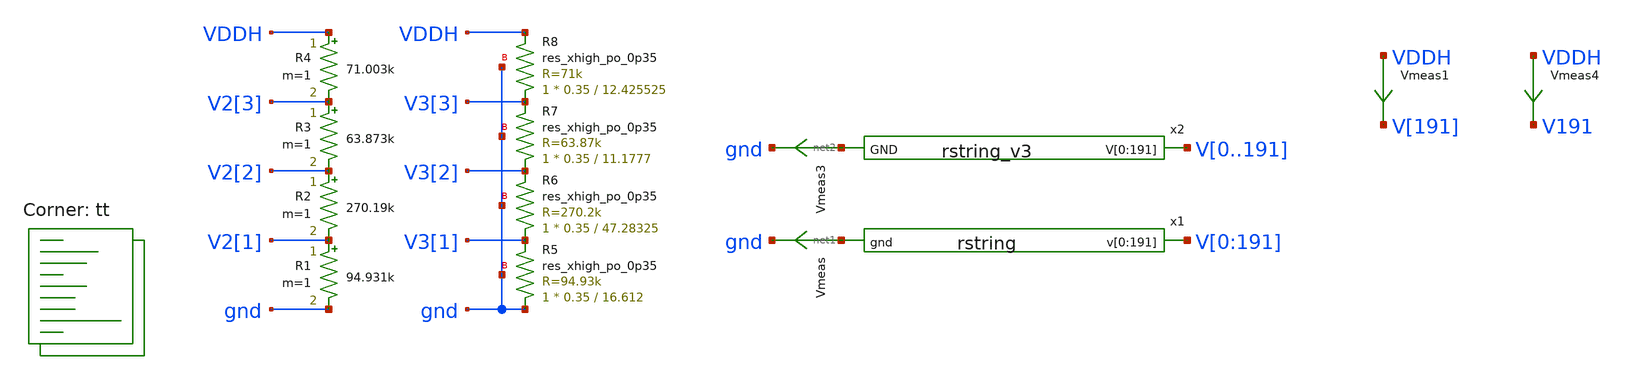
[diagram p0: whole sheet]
** sch_path: xschem/res_seg-tb.sch
**.subckt res_seg-tb
x1 V[0] V[1] V[2] V[3] V[4] V[5] V[6] V[7] V[8] V[9] V[10] V[11] V[12] V[13] V[14] V[15] V[16] V[17]
+ V[18] V[19] V[20] V[21] V[22] V[23] V[24] V[25] V[26] V[27] V[28] V[29] V[30] V[31] V[32] V[33] V[34]
+ V[35] V[36] V[37] V[38] V[39] V[40] V[41] V[42] V[43] V[44] V[45] V[46] V[47] V[48] V[49] V[50] V[51]
+ V[52] V[53] V[54] V[55] V[56] V[57] V[58] V[59] V[60] V[61] V[62] V[63] V[64] V[65] V[66] V[67] V[68]
+ V[69] V[70] V[71] V[72] V[73] V[74] V[75] V[76] V[77] V[78] V[79] V[80] V[81] V[82] V[83] V[84] V[85]
+ V[86] V[87] V[88] V[89] V[90] V[91] V[92] V[93] V[94] V[95] V[96] V[97] V[98] V[99] V[100] V[101] V[102]
+ V[103] V[104] V[105] V[106] V[107] V[108] V[109] V[110] V[111] V[112] V[113] V[114] V[115] V[116] V[117]
+ V[118] V[119] V[120] V[121] V[122] V[123] V[124] V[125] V[126] V[127] V[128] V[129] V[130] V[131] V[132]
+ V[133] V[134] V[135] V[136] V[137] V[138] V[139] V[140] V[141] V[142] V[143] V[144] V[145] V[146] V[147]
+ V[148] V[149] V[150] V[151] V[152] V[153] V[154] V[155] V[156] V[157] V[158] V[159] V[160] V[161] V[162]
+ V[163] V[164] V[165] V[166] V[167] V[168] V[169] V[170] V[171] V[172] V[173] V[174] V[175] V[176] V[177]
+ V[178] V[179] V[180] V[181] V[182] V[183] V[184] V[185] V[186] V[187] V[188] V[189] V[190] V[191] net1
+ rstring
Vmeas net1 gnd 0
.save i(vmeas)
Vmeas1 VDDH V[191] 0
.save i(vmeas1)
R1 V2[1] gnd 94.931k m=1
R2 V2[2] V2[1] 270.19k m=1
R3 V2[3] V2[2] 63.873k m=1
R4 VDDH V2[3] 71.003k m=1
XR5 gnd V3[1] gnd sky130_fd_pr__res_xhigh_po_0p35 L=16.612 mult=1 m=1
XR6 V3[1] V3[2] gnd sky130_fd_pr__res_xhigh_po_0p35 L=47.28325 mult=1 m=1
XR7 V3[2] V3[3] gnd sky130_fd_pr__res_xhigh_po_0p35 L=11.1777 mult=1 m=1
XR8 V3[3] VDDH gnd sky130_fd_pr__res_xhigh_po_0p35 L=12.425525 mult=1 m=1
Vmeas3 net2 gnd 0
.save i(vmeas3)
x2 V0 V1 V2 V3 V4 V5 V6 V7 V8 V9 V10 V11 V12 V13 V14 V15 V16 V17 V18 V19 V20 V21 V22 V23 V24 V25 V26
+ V27 V28 V29 V30 V31 V32 V33 V34 V35 V36 V37 V38 V39 V40 V41 V42 V43 V44 V45 V46 V47 V48 V49 V50 V51 V52
+ V53 V54 V55 V56 V57 V58 V59 V60 V61 V62 V63 V64 V65 V66 V67 V68 V69 V70 V71 V72 V73 V74 V75 V76 V77 V78
+ V79 V80 V81 V82 V83 V84 V85 V86 V87 V88 V89 V90 V91 V92 V93 V94 V95 V96 V97 V98 V99 V100 V101 V102 V103
+ V104 V105 V106 V107 V108 V109 V110 V111 V112 V113 V114 V115 V116 V117 V118 V119 V120 V121 V122 V123 V124
+ V125 V126 V127 V128 V129 V130 V131 V132 V133 V134 V135 V136 V137 V138 V139 V140 V141 V142 V143 V144 V145
+ V146 V147 V148 V149 V150 V151 V152 V153 V154 V155 V156 V157 V158 V159 V160 V161 V162 V163 V164 V165 V166
+ V167 V168 V169 V170 V171 V172 V173 V174 V175 V176 V177 V178 V179 V180 V181 V182 V183 V184 V185 V186 V187
+ V188 V189 V190 V191 net2 rstring_v3
Vmeas4 VDDH V191 0
.save i(vmeas4)
**** begin user architecture code



  .include $THESIS_WS/spice/header.spice
  .option wnflag=1
  .option safecurrents
  ********************Static Voltage Sources***************************
  Vddh vddh gnd dc 5.5
  v0 v[0] gnd 0
  *v191 v[191] gnd 5.5

  *v1_191 v1[191] gnd 5.5
  v1_0 v0 gnd 0

  Vdm dm gnd 0
  ********************Dynamic Voltage Sources***************************
  *******Calculation**********
  .param base_f=100e3 base_t={1/base_f} base_th={base_t/2} base_d={base_th}
  .param d2_th ={base_th} d2_t={d1_th}
  .param d1_th ={4*d2_th} d1_t={d0_th}
  .param d0_th ={4*d1_th} d0_t={4*d0_th}

  .param d20_d ={0} d21_d={1*d2_th} d22_d={2*d2_th} d23_d={3*d2_th}
  .param d10_d ={0} d11_d={1*d1_th} d12_d={2*d1_th} d13_d={3*d1_th}
  .param d00_d ={0} d01_d={1*d0_th} d02_d={2*d0_th} d03_d={3*d0_th}
  *******Signals**********
  .param vhi=5.5
 * Vd00 d0[0] gnd pulse(0 {vhi} {d00_d} 1n 1n {d0_th} {d0_t})
 * Vd01 d0[1] gnd pulse(0 {vhi} {d01_d} 1n 1n {d0_th} {d0_t})
 * Vd02 d0[2] gnd pulse(0 {vhi} {d02_d} 1n 1n {d0_th} {d0_t})
 * Vd03 d0[3] gnd pulse(0 {vhi} {d03_d} 1n 1n {d0_th} {d0_t})

 * Vd10 d1[0] gnd pulse(0 {vhi} {d10_d} 1n 1n {d1_th} {d1_t})
 * Vd11 d1[1] gnd pulse(0 {vhi} {d11_d} 1n 1n {d1_th} {d1_t})
 * Vd12 d1[2] gnd pulse(0 {vhi} {d12_d} 1n 1n {d1_th} {d1_t})
 * Vd13 d1[3] gnd pulse(0 {vhi} {d13_d} 1n 1n {d1_th} {d1_t})

 * Vd20 d2[0] gnd pulse(0 {vhi} {d20_d} 1n 1n {d2_th} {d2_t})
 * Vd21 d2[1] gnd pulse(0 {vhi} {d21_d} 1n 1n {d2_th} {d2_t})
 * Vd22 d2[2] gnd pulse(0 {vhi} {d22_d} 1n 1n {d2_th} {d2_t})
 * Vd23 d2[3] gnd pulse(0 {vhi} {d23_d} 1n 1n {d2_th} {d2_t})
  ********************Simulation Commands*****************************
  .control
     reset
     *save all
     *tran 1u 10u
     dc Vdm 0 1 1
     write res_seg-tb.raw
     set wr_singlescale
     set wr_vecnames
     wrdata $THESIS_WS/simulations/rseg-tb11.txt dc.all


*     dc Vdm 0 1 1
*     write res_seg-tb.raw
*    quit 0
  .endc



.lib $::SKYWATER_MODELS/sky130.lib.spice tt


.save v1 v2 v3 v4 v5 v6 v7 v8 v9 v10
.save v11 v12 v13 v14 v15 v16 v17 v18 v19 v20
.save v21 v22 v23 v24 v25 v26 v27 v28 v29 v30
.save v31 v32 v33 v34 v35 v36 v37 v38 v39 v40
.save v41 v42 v43 v44 v45 v46 v47 v48 v49 v50
.save v51 v52 v53 v54 v55 v56 v57 v58 v59 v60
.save v61 v62 v63 v64 v65 v66 v67 v68 v69 v70
.save v71 v72 v73 v74 v75 v76 v77 v78 v79 v80
.save v81 v82 v83 v84 v85 v86 v87 v88 v89 v90
.save v91 v92 v93 v94 v95 v96 v97 v98 v99 v100
.save v101 v102 v103 v104 v105 v106 v107 v108 v109 v110
.save v111 v112 v113 v114 v115 v116 v117 v118 v119 v120
.save v121 v122 v123 v124 v125 v126 v127 v128 v129 v130
.save v131 v132 v133 v134 v135 v136 v137 v138 v139 v140
.save v141 v142 v143 v144 v145 v146 v147 v148 v149 v150
.save v151 v152 v153 v154 v155 v156 v157 v158 v159 v160
.save v161 v162 v163 v164 v165 v166 v167 v168 v169 v170
.save v171 v172 v173 v174 v175 v176 v177 v178 v179 v180
.save v181 v182 v183 v184 v185 v186 v187 v188 v189 v190
.save v191


**** end user architecture code
**.ends

* expanding   symbol:  rstring.sym # of pins=2
** sym_path: xschem/rstring.sym
** sch_path: xschem/rstring.sch
.subckt rstring v[0] v[1] v[2] v[3] v[4] v[5] v[6] v[7] v[8] v[9] v[10] v[11] v[12] v[13] v[14]
+ v[15] v[16] v[17] v[18] v[19] v[20] v[21] v[22] v[23] v[24] v[25] v[26] v[27] v[28] v[29] v[30] v[31]
+ v[32] v[33] v[34] v[35] v[36] v[37] v[38] v[39] v[40] v[41] v[42] v[43] v[44] v[45] v[46] v[47] v[48]
+ v[49] v[50] v[51] v[52] v[53] v[54] v[55] v[56] v[57] v[58] v[59] v[60] v[61] v[62] v[63] v[64] v[65]
+ v[66] v[67] v[68] v[69] v[70] v[71] v[72] v[73] v[74] v[75] v[76] v[77] v[78] v[79] v[80] v[81] v[82]
+ v[83] v[84] v[85] v[86] v[87] v[88] v[89] v[90] v[91] v[92] v[93] v[94] v[95] v[96] v[97] v[98] v[99]
+ v[100] v[101] v[102] v[103] v[104] v[105] v[106] v[107] v[108] v[109] v[110] v[111] v[112] v[113] v[114]
+ v[115] v[116] v[117] v[118] v[119] v[120] v[121] v[122] v[123] v[124] v[125] v[126] v[127] v[128] v[129]
+ v[130] v[131] v[132] v[133] v[134] v[135] v[136] v[137] v[138] v[139] v[140] v[141] v[142] v[143] v[144]
+ v[145] v[146] v[147] v[148] v[149] v[150] v[151] v[152] v[153] v[154] v[155] v[156] v[157] v[158] v[159]
+ v[160] v[161] v[162] v[163] v[164] v[165] v[166] v[167] v[168] v[169] v[170] v[171] v[172] v[173] v[174]
+ v[175] v[176] v[177] v[178] v[179] v[180] v[181] v[182] v[183] v[184] v[185] v[186] v[187] v[188] v[189]
+ v[190] v[191] gnd
*.opin
*+ v[0],v[1],v[2],v[3],v[4],v[5],v[6],v[7],v[8],v[9],v[10],v[11],v[12],v[13],v[14],v[15],v[16],v[17],v[18],v[19],v[20],v[21],v[22],v[23],v[24],v[25],v[26],v[27],v[28],v[29],v[30],v[31],v[32],v[33],v[34],v[35],v[36],v[37],v[38],v[39],v[40],v[41],v[42],v[43],v[44],v[45],v[46],v[47],v[48],v[49],v[50],v[51],v[52],v[53],v[54],v[55],v[56],v[57],v[58],v[59],v[60],v[61],v[62],v[63],v[64],v[65],v[66],v[67],v[68],v[69],v[70],v[71],v[72],v[73],v[74],v[75],v[76],v[77],v[78],v[79],v[80],v[81],v[82],v[83],v[84],v[85],v[86],v[87],v[88],v[89],v[90],v[91],v[92],v[93],v[94],v[95],v[96],v[97],v[98],v[99],v[100],v[101],v[102],v[103],v[104],v[105],v[106],v[107],v[108],v[109],v[110],v[111],v[112],v[113],v[114],v[115],v[116],v[117],v[118],v[119],v[120],v[121],v[122],v[123],v[124],v[125],v[126],v[127],v[128],v[129],v[130],v[131],v[132],v[133],v[134],v[135],v[136],v[137],v[138],v[139],v[140],v[141],v[142],v[143],v[144],v[145],v[146],v[147],v[148],v[149],v[150],v[151],v[152],v[153],v[154],v[155],v[156],v[157],v[158],v[159],v[160],v[161],v[162],v[163],v[164],v[165],v[166],v[167],v[168],v[169],v[170],v[171],v[172],v[173],v[174],v[175],v[176],v[177],v[178],v[179],v[180],v[181],v[182],v[183],v[184],v[185],v[186],v[187],v[188],v[189],v[190],v[191]
*.ipin gnd
x1 v[0] v[1] v[2] v[3] v[4] v[5] v[6] v[7] v[8] v[9] v[10] v[11] v[12] v[13] v[14] v[15] v[16] v[17]
+ v[18] v[19] v[20] v[21] v[22] v[23] v[24] v[25] v[26] v[27] v[28] v[29] v[30] v[31] v[32] v[33] v[34]
+ v[35] v[36] v[37] v[38] v[39] v[40] v[41] v[42] v[43] v[44] v[45] v[46] v[47] v[48] v[49] v[50] v[51]
+ v[52] v[53] v[54] v[55] v[56] v[57] v[58] v[59] v[60] v[61] v[62] v[63] v[64] gnd res_seg_1
x2 v[64] v[65] v[66] v[67] v[68] v[69] v[70] v[71] v[72] v[73] v[74] v[75] v[76] v[77] v[78] v[79]
+ v[80] v[81] v[82] v[83] v[84] v[85] v[86] v[87] v[88] v[89] v[90] v[91] v[92] v[93] v[94] v[95] v[96]
+ v[97] v[98] v[99] v[100] v[101] v[102] v[103] v[104] v[105] v[106] v[107] v[108] v[109] v[110] v[111]
+ v[112] gnd res_seg_2
x3 v[112] v[113] v[114] v[115] v[116] v[117] v[118] v[119] v[120] v[121] v[122] v[123] v[124] v[125]
+ v[126] v[127] v[128] gnd res_seg_3
x4 v[128] v[129] v[130] v[131] v[132] v[133] v[134] v[135] v[136] v[137] v[138] v[139] v[140] v[141]
+ v[142] v[143] v[144] v[145] v[146] v[147] v[148] v[149] v[150] v[151] v[152] v[153] v[154] v[155] v[156]
+ v[157] v[158] v[159] v[160] v[161] v[162] v[163] v[164] v[165] v[166] v[167] v[168] v[169] v[170] v[171]
+ v[172] v[173] v[174] v[175] v[176] v[177] v[178] v[179] v[180] v[181] v[182] v[183] v[184] v[185] v[186]
+ v[187] v[188] v[189] v[190] v[191] gnd res_seg_4
.ends


* expanding   symbol:  rstring_v3.sym # of pins=2
** sym_path: xschem/rstring_v3.sym
** sch_path: xschem/rstring_v3.sch
.subckt rstring_v3 V[0] V[1] V[2] V[3] V[4] V[5] V[6] V[7] V[8] V[9] V[10] V[11] V[12] V[13] V[14]
+ V[15] V[16] V[17] V[18] V[19] V[20] V[21] V[22] V[23] V[24] V[25] V[26] V[27] V[28] V[29] V[30] V[31]
+ V[32] V[33] V[34] V[35] V[36] V[37] V[38] V[39] V[40] V[41] V[42] V[43] V[44] V[45] V[46] V[47] V[48]
+ V[49] V[50] V[51] V[52] V[53] V[54] V[55] V[56] V[57] V[58] V[59] V[60] V[61] V[62] V[63] V[64] V[65]
+ V[66] V[67] V[68] V[69] V[70] V[71] V[72] V[73] V[74] V[75] V[76] V[77] V[78] V[79] V[80] V[81] V[82]
+ V[83] V[84] V[85] V[86] V[87] V[88] V[89] V[90] V[91] V[92] V[93] V[94] V[95] V[96] V[97] V[98] V[99]
+ V[100] V[101] V[102] V[103] V[104] V[105] V[106] V[107] V[108] V[109] V[110] V[111] V[112] V[113] V[114]
+ V[115] V[116] V[117] V[118] V[119] V[120] V[121] V[122] V[123] V[124] V[125] V[126] V[127] V[128] V[129]
+ V[130] V[131] V[132] V[133] V[134] V[135] V[136] V[137] V[138] V[139] V[140] V[141] V[142] V[143] V[144]
+ V[145] V[146] V[147] V[148] V[149] V[150] V[151] V[152] V[153] V[154] V[155] V[156] V[157] V[158] V[159]
+ V[160] V[161] V[162] V[163] V[164] V[165] V[166] V[167] V[168] V[169] V[170] V[171] V[172] V[173] V[174]
+ V[175] V[176] V[177] V[178] V[179] V[180] V[181] V[182] V[183] V[184] V[185] V[186] V[187] V[188] V[189]
+ V[190] V[191] GND
*.opin
*+ V[0],V[1],V[2],V[3],V[4],V[5],V[6],V[7],V[8],V[9],V[10],V[11],V[12],V[13],V[14],V[15],V[16],V[17],V[18],V[19],V[20],V[21],V[22],V[23],V[24],V[25],V[26],V[27],V[28],V[29],V[30],V[31],V[32],V[33],V[34],V[35],V[36],V[37],V[38],V[39],V[40],V[41],V[42],V[43],V[44],V[45],V[46],V[47],V[48],V[49],V[50],V[51],V[52],V[53],V[54],V[55],V[56],V[57],V[58],V[59],V[60],V[61],V[62],V[63],V[64],V[65],V[66],V[67],V[68],V[69],V[70],V[71],V[72],V[73],V[74],V[75],V[76],V[77],V[78],V[79],V[80],V[81],V[82],V[83],V[84],V[85],V[86],V[87],V[88],V[89],V[90],V[91],V[92],V[93],V[94],V[95],V[96],V[97],V[98],V[99],V[100],V[101],V[102],V[103],V[104],V[105],V[106],V[107],V[108],V[109],V[110],V[111],V[112],V[113],V[114],V[115],V[116],V[117],V[118],V[119],V[120],V[121],V[122],V[123],V[124],V[125],V[126],V[127],V[128],V[129],V[130],V[131],V[132],V[133],V[134],V[135],V[136],V[137],V[138],V[139],V[140],V[141],V[142],V[143],V[144],V[145],V[146],V[147],V[148],V[149],V[150],V[151],V[152],V[153],V[154],V[155],V[156],V[157],V[158],V[159],V[160],V[161],V[162],V[163],V[164],V[165],V[166],V[167],V[168],V[169],V[170],V[171],V[172],V[173],V[174],V[175],V[176],V[177],V[178],V[179],V[180],V[181],V[182],V[183],V[184],V[185],V[186],V[187],V[188],V[189],V[190],V[191]
*.ipin GND
x1 V[0] V[1] V[2] V[3] V[4] V[5] V[6] V[7] V[8] V[9] V[10] V[11] V[12] V[13] V[14] V[15] V[16] V[17]
+ V[18] V[19] V[20] V[21] V[22] V[23] V[24] V[25] V[26] V[27] V[28] V[29] V[30] V[31] V[32] V[33] V[34]
+ V[35] V[36] V[37] V[38] V[39] V[40] V[41] V[42] V[43] V[44] V[45] V[46] V[47] V[48] V[49] V[50] V[51]
+ V[52] V[53] V[54] V[55] V[56] V[57] V[58] V[59] V[60] V[61] V[62] V[63] V[64] GND rseg_1_v3
x2 V[64] V[65] V[66] V[67] V[68] V[69] V[70] V[71] V[72] V[73] V[74] V[75] V[76] V[77] V[78] V[79]
+ V[80] V[81] V[82] V[83] V[84] V[85] V[86] V[87] V[88] V[89] V[90] V[91] V[92] V[93] V[94] V[95] V[96]
+ V[97] V[98] V[99] V[100] V[101] V[102] V[103] V[104] V[105] V[106] V[107] V[108] V[109] V[110] V[111]
+ V[112] GND rseg_2_v3
x3 V[112] V[113] V[114] V[115] V[116] V[117] V[118] V[119] V[120] V[121] V[122] V[123] V[124] V[125]
+ V[126] V[127] V[128] GND rseg_3_v3
x4 V[128] V[129] V[130] V[131] V[132] V[133] V[134] V[135] V[136] V[137] V[138] V[139] V[140] V[141]
+ V[142] V[143] V[144] V[145] V[146] V[147] V[148] V[149] V[150] V[151] V[152] V[153] V[154] V[155] V[156]
+ V[157] V[158] V[159] V[160] V[161] V[162] V[163] V[164] V[165] V[166] V[167] V[168] V[169] V[170] V[171]
+ V[172] V[173] V[174] V[175] V[176] V[177] V[178] V[179] V[180] V[181] V[182] V[183] V[184] V[185] V[186]
+ V[187] V[188] V[189] V[190] V[191] GND rseg_4_v3
.ends


* expanding   symbol:  res_seg_1.sym # of pins=2
** sym_path: xschem/res_seg_1.sym
** sch_path: xschem/res_seg_1.sch
.subckt res_seg_1 v[0] v[1] v[2] v[3] v[4] v[5] v[6] v[7] v[8] v[9] v[10] v[11] v[12] v[13] v[14]
+ v[15] v[16] v[17] v[18] v[19] v[20] v[21] v[22] v[23] v[24] v[25] v[26] v[27] v[28] v[29] v[30] v[31]
+ v[32] v[33] v[34] v[35] v[36] v[37] v[38] v[39] v[40] v[41] v[42] v[43] v[44] v[45] v[46] v[47] v[48]
+ v[49] v[50] v[51] v[52] v[53] v[54] v[55] v[56] v[57] v[58] v[59] v[60] v[61] v[62] v[63] v[64] gnd
*.opin
*+ v[0],v[1],v[2],v[3],v[4],v[5],v[6],v[7],v[8],v[9],v[10],v[11],v[12],v[13],v[14],v[15],v[16],v[17],v[18],v[19],v[20],v[21],v[22],v[23],v[24],v[25],v[26],v[27],v[28],v[29],v[30],v[31],v[32],v[33],v[34],v[35],v[36],v[37],v[38],v[39],v[40],v[41],v[42],v[43],v[44],v[45],v[46],v[47],v[48],v[49],v[50],v[51],v[52],v[53],v[54],v[55],v[56],v[57],v[58],v[59],v[60],v[61],v[62],v[63],v[64]
*.ipin gnd
XR1 v[1] v[0] gnd sky130_fd_pr__res_xhigh_po_0p35 L=0.8375 mult=1 m=1
XR2 v[2] v[1] gnd sky130_fd_pr__res_xhigh_po_0p35 L=0.7349 mult=1 m=1
XR3 v[3] v[2] gnd sky130_fd_pr__res_xhigh_po_0p35 L=0.6495 mult=1 m=1
XR4 v[4] v[3] gnd sky130_fd_pr__res_xhigh_po_0p35 L=0.5897 mult=1 m=1
XR8 v[7] v[8] gnd sky130_fd_pr__res_xhigh_po_0p69 L=0.8761 mult=1 m=1
XR9 v[8] v[9] gnd sky130_fd_pr__res_xhigh_po_0p69 L=0.8255 mult=1 m=1
XR10 v[9] v[10] gnd sky130_fd_pr__res_xhigh_po_0p69 L=0.775 mult=1 m=1
XR11 v[10] v[11] gnd sky130_fd_pr__res_xhigh_po_0p69 L=0.7413 mult=1 m=1
XR12 v[11] v[12] gnd sky130_fd_pr__res_xhigh_po_0p69 L=0.7076 mult=1 m=1
XR13 v[12] v[13] gnd sky130_fd_pr__res_xhigh_po_0p69 L=0.6739 mult=1 m=1
XR14 v[13] v[14] gnd sky130_fd_pr__res_xhigh_po_0p69 L=0.657 mult=1 m=1
XR15 v[14] v[15] gnd sky130_fd_pr__res_xhigh_po_0p69 L=0.6234 mult=1 m=1
XR16 v[15] v[16] gnd sky130_fd_pr__res_xhigh_po_0p69 L=0.6065 mult=1 m=1
XR17 v[16] v[17] gnd sky130_fd_pr__res_xhigh_po_0p69 L=0.5728 mult=1 m=1
XR19 v[18] v[19] gnd sky130_fd_pr__res_xhigh_po_0p69 L=0.5391 mult=1 m=1
XR27 v[26] v[27] gnd sky130_fd_pr__res_xhigh_po_1p41 L=0.8951 mult=1 m=1
XR29 v[28] v[29] gnd sky130_fd_pr__res_xhigh_po_1p41 L=0.8607 mult=1 m=1
XR31 v[30] v[31] gnd sky130_fd_pr__res_xhigh_po_1p41 L=0.8263 mult=1 m=1
XR33 v[32] v[33] gnd sky130_fd_pr__res_xhigh_po_1p41 L=0.7918 mult=1 m=1
XR36 v[35] v[36] gnd sky130_fd_pr__res_xhigh_po_1p41 L=0.7574 mult=1 m=1
XR37 v[36] v[37] gnd sky130_fd_pr__res_xhigh_po_1p41 L=0.723 mult=1 m=1
XR40 v[39] v[40] gnd sky130_fd_pr__res_xhigh_po_1p41 L=0.6885 mult=1 m=1
XR41 v[40] v[41] gnd sky130_fd_pr__res_xhigh_po_1p41 L=0.723 mult=1 m=1
XR42 v[41] v[42] gnd sky130_fd_pr__res_xhigh_po_1p41 L=0.6885 mult=1 m=1
XR43 v[42] v[43] gnd sky130_fd_pr__res_xhigh_po_1p41 L=0.6541 mult=1 m=1
XR45 v[44] v[45] gnd sky130_fd_pr__res_xhigh_po_1p41 L=0.6541 mult=1 m=1
XR48 v[47] v[48] gnd sky130_fd_pr__res_xhigh_po_1p41 L=0.6197 mult=1 m=1
XR49 v[48] v[49] gnd sky130_fd_pr__res_xhigh_po_1p41 L=0.6541 mult=1 m=1
XR51 v[50] v[51] gnd sky130_fd_pr__res_xhigh_po_1p41 L=0.5853 mult=1 m=1
XR52 v[51] v[52] gnd sky130_fd_pr__res_xhigh_po_1p41 L=0.6197 mult=1 m=1
XR53 v[52] v[53] gnd sky130_fd_pr__res_xhigh_po_1p41 L=0.5853 mult=1 m=1
XR58 v[57] v[58] gnd sky130_fd_pr__res_xhigh_po_1p41 L=0.5508 mult=1 m=1
XR64 v[63] v[64] gnd sky130_fd_pr__res_xhigh_po_1p41 L=0.5164 mult=1 m=1
XR5 v[5] v[4] gnd sky130_fd_pr__res_xhigh_po_0p35 L=0.5469 mult=1 m=1
XR6 v[6] v[5] gnd sky130_fd_pr__res_xhigh_po_0p35 L=0.5042 mult=1 m=1
XR21 v[20] v[21] gnd sky130_fd_pr__res_xhigh_po_0p69 L=0.5054 mult=1 m=1
XR54 v[53] v[54] gnd sky130_fd_pr__res_xhigh_po_1p41 L=0.5853 mult=1 m=1
XR7 v[6] v[7] gnd sky130_fd_pr__res_xhigh_po_0p69 L=0.9266 mult=1 m=1
XR18 v[17] v[18] gnd sky130_fd_pr__res_xhigh_po_0p69 L=0.5728 mult=1 m=1
XR20 v[19] v[20] gnd sky130_fd_pr__res_xhigh_po_0p69 L=0.5391 mult=1 m=1
XR22 v[21] v[22] gnd sky130_fd_pr__res_xhigh_po_0p69 L=0.5054 mult=1 m=1
XR23 v[22] v[23] gnd sky130_fd_pr__res_xhigh_po_1p41 L=0.9984 mult=1 m=1
XR24 v[23] v[24] gnd sky130_fd_pr__res_xhigh_po_1p41 L=0.9984 mult=1 m=1
XR25 v[24] v[25] gnd sky130_fd_pr__res_xhigh_po_1p41 L=0.9295 mult=1 m=1
XR26 v[25] v[26] gnd sky130_fd_pr__res_xhigh_po_1p41 L=0.9295 mult=1 m=1
XR28 v[27] v[28] gnd sky130_fd_pr__res_xhigh_po_1p41 L=0.8951 mult=1 m=1
XR30 v[29] v[30] gnd sky130_fd_pr__res_xhigh_po_1p41 L=0.8607 mult=1 m=1
XR32 v[31] v[32] gnd sky130_fd_pr__res_xhigh_po_1p41 L=0.8263 mult=1 m=1
XR34 v[33] v[34] gnd sky130_fd_pr__res_xhigh_po_1p41 L=0.7918 mult=1 m=1
XR35 v[34] v[35] gnd sky130_fd_pr__res_xhigh_po_1p41 L=0.7918 mult=1 m=1
XR38 v[37] v[38] gnd sky130_fd_pr__res_xhigh_po_1p41 L=0.7574 mult=1 m=1
XR39 v[38] v[39] gnd sky130_fd_pr__res_xhigh_po_1p41 L=0.723 mult=1 m=1
XR44 v[43] v[44] gnd sky130_fd_pr__res_xhigh_po_1p41 L=0.6885 mult=1 m=1
XR46 v[45] v[46] gnd sky130_fd_pr__res_xhigh_po_1p41 L=0.6541 mult=1 m=1
XR47 v[46] v[47] gnd sky130_fd_pr__res_xhigh_po_1p41 L=0.6541 mult=1 m=1
XR50 v[49] v[50] gnd sky130_fd_pr__res_xhigh_po_1p41 L=0.6197 mult=1 m=1
XR55 v[54] v[55] gnd sky130_fd_pr__res_xhigh_po_1p41 L=0.5853 mult=1 m=1
XR56 v[55] v[56] gnd sky130_fd_pr__res_xhigh_po_1p41 L=0.5853 mult=1 m=1
XR57 v[56] v[57] gnd sky130_fd_pr__res_xhigh_po_1p41 L=0.5853 mult=1 m=1
XR59 v[58] v[59] gnd sky130_fd_pr__res_xhigh_po_1p41 L=0.5508 mult=1 m=1
XR60 v[59] v[60] gnd sky130_fd_pr__res_xhigh_po_1p41 L=0.5508 mult=1 m=1
XR61 v[60] v[61] gnd sky130_fd_pr__res_xhigh_po_1p41 L=0.5508 mult=1 m=1
XR62 v[61] v[62] gnd sky130_fd_pr__res_xhigh_po_1p41 L=0.5508 mult=1 m=1
XR63 v[62] v[63] gnd sky130_fd_pr__res_xhigh_po_1p41 L=0.5508 mult=1 m=1
.ends


* expanding   symbol:  res_seg_2.sym # of pins=2
** sym_path: xschem/res_seg_2.sym
** sch_path: xschem/res_seg_2.sch
.subckt res_seg_2 v[0] v[1] v[2] v[3] v[4] v[5] v[6] v[7] v[8] v[9] v[10] v[11] v[12] v[13] v[14]
+ v[15] v[16] v[17] v[18] v[19] v[20] v[21] v[22] v[23] v[24] v[25] v[26] v[27] v[28] v[29] v[30] v[31]
+ v[32] v[33] v[34] v[35] v[36] v[37] v[38] v[39] v[40] v[41] v[42] v[43] v[44] v[45] v[46] v[47] v[48] gnd
*.opin
*+ v[0],v[1],v[2],v[3],v[4],v[5],v[6],v[7],v[8],v[9],v[10],v[11],v[12],v[13],v[14],v[15],v[16],v[17],v[18],v[19],v[20],v[21],v[22],v[23],v[24],v[25],v[26],v[27],v[28],v[29],v[30],v[31],v[32],v[33],v[34],v[35],v[36],v[37],v[38],v[39],v[40],v[41],v[42],v[43],v[44],v[45],v[46],v[47],v[48]
*.ipin gnd
XR1 v[1] v[0] gnd sky130_fd_pr__res_xhigh_po_0p35 L=1.9570 mult=1 m=1
XR2 v[2] v[1] gnd sky130_fd_pr__res_xhigh_po_0p35 L=1.7348 mult=1 m=1
XR3 v[3] v[2] gnd sky130_fd_pr__res_xhigh_po_0p35 L=1.5639 mult=1 m=1
XR4 v[4] v[3] gnd sky130_fd_pr__res_xhigh_po_0p35 L=1.4442 mult=1 m=1
XR5 v[5] v[4] gnd sky130_fd_pr__res_xhigh_po_0p35 L=1.3417 mult=1 m=1
XR6 v[6] v[5] gnd sky130_fd_pr__res_xhigh_po_0p35 L=1.2648 mult=1 m=1
XR7 v[7] v[6] gnd sky130_fd_pr__res_xhigh_po_0p35 L=1.1964 mult=1 m=1
XR8 v[8] v[7] gnd sky130_fd_pr__res_xhigh_po_0p35 L=1.1366 mult=1 m=1
XR9 v[9] v[8] gnd sky130_fd_pr__res_xhigh_po_0p35 L=1.0853 mult=1 m=1
XR10 v[10] v[9] gnd sky130_fd_pr__res_xhigh_po_0p35 L=1.0511 mult=1 m=1
XR11 v[11] v[10] gnd sky130_fd_pr__res_xhigh_po_0p35 L=1.0169 mult=1 m=1
XR12 v[12] v[11] gnd sky130_fd_pr__res_xhigh_po_0p35 L=0.9828 mult=1 m=1
XR13 v[13] v[12] gnd sky130_fd_pr__res_xhigh_po_0p35 L=0.9571 mult=1 m=1
XR14 v[14] v[13] gnd sky130_fd_pr__res_xhigh_po_0p35 L=0.94 mult=1 m=1
XR15 v[15] v[14] gnd sky130_fd_pr__res_xhigh_po_0p35 L=0.9144 mult=1 m=1
XR16 v[16] v[15] gnd sky130_fd_pr__res_xhigh_po_0p35 L=0.8888 mult=1 m=1
XR17 v[17] v[16] gnd sky130_fd_pr__res_xhigh_po_0p35 L=0.8802 mult=1 m=1
XR18 v[18] v[17] gnd sky130_fd_pr__res_xhigh_po_0p35 L=0.8717 mult=1 m=1
XR19 v[19] v[18] gnd sky130_fd_pr__res_xhigh_po_0p35 L=0.8546 mult=1 m=1
XR20 v[20] v[19] gnd sky130_fd_pr__res_xhigh_po_0p35 L=0.8375 mult=1 m=1
XR22 v[22] v[21] gnd sky130_fd_pr__res_xhigh_po_0p35 L=0.8289 mult=1 m=1
XR23 v[23] v[22] gnd sky130_fd_pr__res_xhigh_po_0p35 L=0.8204 mult=1 m=1
XR24 v[24] v[23] gnd sky130_fd_pr__res_xhigh_po_0p35 L=0.8118 mult=1 m=1
XR33 v[33] v[32] gnd sky130_fd_pr__res_xhigh_po_0p35 L=0.8204 mult=1 m=1
XR35 v[35] v[34] gnd sky130_fd_pr__res_xhigh_po_0p35 L=0.8289 mult=1 m=1
XR36 v[36] v[35] gnd sky130_fd_pr__res_xhigh_po_0p35 L=0.8375 mult=1 m=1
XR38 v[38] v[37] gnd sky130_fd_pr__res_xhigh_po_0p35 L=0.8631 mult=1 m=1
XR40 v[40] v[39] gnd sky130_fd_pr__res_xhigh_po_0p35 L=0.8888 mult=1 m=1
XR41 v[41] v[40] gnd sky130_fd_pr__res_xhigh_po_0p35 L=0.8973 mult=1 m=1
XR42 v[42] v[41] gnd sky130_fd_pr__res_xhigh_po_0p35 L=0.9144 mult=1 m=1
XR43 v[43] v[42] gnd sky130_fd_pr__res_xhigh_po_0p35 L=0.94 mult=1 m=1
XR44 v[44] v[43] gnd sky130_fd_pr__res_xhigh_po_0p35 L=0.9571 mult=1 m=1
XR45 v[45] v[44] gnd sky130_fd_pr__res_xhigh_po_0p35 L=0.9828 mult=1 m=1
XR46 v[46] v[45] gnd sky130_fd_pr__res_xhigh_po_0p35 L=1.0084 mult=1 m=1
XR47 v[47] v[46] gnd sky130_fd_pr__res_xhigh_po_0p35 L=1.0426 mult=1 m=1
XR48 v[48] v[47] gnd sky130_fd_pr__res_xhigh_po_0p35 L=1.0853 mult=1 m=1
XR37 v[37] v[36] gnd sky130_fd_pr__res_xhigh_po_0p35 L=0.846 mult=1 m=1
XR21 v[21] v[20] gnd sky130_fd_pr__res_xhigh_po_0p35 L=0.8375 mult=1 m=1
XR25 v[25] v[24] gnd sky130_fd_pr__res_xhigh_po_0p35 L=0.8118 mult=1 m=1
XR26 v[26] v[25] gnd sky130_fd_pr__res_xhigh_po_0p35 L=0.8118 mult=1 m=1
XR27 v[27] v[26] gnd sky130_fd_pr__res_xhigh_po_0p35 L=0.8033 mult=1 m=1
XR28 v[28] v[27] gnd sky130_fd_pr__res_xhigh_po_0p35 L=0.8118 mult=1 m=1
XR29 v[29] v[28] gnd sky130_fd_pr__res_xhigh_po_0p35 L=0.8033 mult=1 m=1
XR30 v[30] v[29] gnd sky130_fd_pr__res_xhigh_po_0p35 L=0.8033 mult=1 m=1
XR31 v[31] v[30] gnd sky130_fd_pr__res_xhigh_po_0p35 L=0.8118 mult=1 m=1
XR32 v[32] v[31] gnd sky130_fd_pr__res_xhigh_po_0p35 L=0.8118 mult=1 m=1
XR34 v[34] v[33] gnd sky130_fd_pr__res_xhigh_po_0p35 L=0.8204 mult=1 m=1
XR39 v[39] v[38] gnd sky130_fd_pr__res_xhigh_po_0p35 L=0.8631 mult=1 m=1
.ends


* expanding   symbol:  res_seg_3.sym # of pins=2
** sym_path: xschem/res_seg_3.sym
** sch_path: xschem/res_seg_3.sch
.subckt res_seg_3 v[0] v[1] v[2] v[3] v[4] v[5] v[6] v[7] v[8] v[9] v[10] v[11] v[12] v[13] v[14]
+ v[15] v[16] gnd
*.opin v[0],v[1],v[2],v[3],v[4],v[5],v[6],v[7],v[8],v[9],v[10],v[11],v[12],v[13],v[14],v[15],v[16]
*.ipin gnd
XR1 v[0] v[1] gnd sky130_fd_pr__res_xhigh_po_0p35 L=0.5555 mult=1 m=1
XR2 v[1] v[2] gnd sky130_fd_pr__res_xhigh_po_0p35 L=0.5726 mult=1 m=1
XR3 v[2] v[3] gnd sky130_fd_pr__res_xhigh_po_0p35 L=0.5811 mult=1 m=1
XR4 v[3] v[4] gnd sky130_fd_pr__res_xhigh_po_0p35 L=0.5897 mult=1 m=1
XR5 v[4] v[5] gnd sky130_fd_pr__res_xhigh_po_0p35 L=0.6153 mult=1 m=1
XR6 v[5] v[6] gnd sky130_fd_pr__res_xhigh_po_0p35 L=0.6238 mult=1 m=1
XR7 v[6] v[7] gnd sky130_fd_pr__res_xhigh_po_0p35 L=0.6409 mult=1 m=1
XR8 v[7] v[8] gnd sky130_fd_pr__res_xhigh_po_0p35 L=0.6666 mult=1 m=1
XR9 v[8] v[9] gnd sky130_fd_pr__res_xhigh_po_0p35 L=0.6837 mult=1 m=1
XR10 v[9] v[10] gnd sky130_fd_pr__res_xhigh_po_0p35 L=0.7093 mult=1 m=1
XR11 v[10] v[11] gnd sky130_fd_pr__res_xhigh_po_0p35 L=0.7264 mult=1 m=1
XR12 v[11] v[12] gnd sky130_fd_pr__res_xhigh_po_0p35 L=0.7691 mult=1 m=1
XR13 v[12] v[13] gnd sky130_fd_pr__res_xhigh_po_0p35 L=0.7948 mult=1 m=1
XR14 v[13] v[14] gnd sky130_fd_pr__res_xhigh_po_0p35 L=0.8375 mult=1 m=1
XR15 v[14] v[15] gnd sky130_fd_pr__res_xhigh_po_0p35 L=0.8802 mult=1 m=1
XR16 v[15] v[16] gnd sky130_fd_pr__res_xhigh_po_0p35 L=0.9315 mult=1 m=1
.ends


* expanding   symbol:  res_seg_4.sym # of pins=2
** sym_path: xschem/res_seg_4.sym
** sch_path: xschem/res_seg_4.sch
.subckt res_seg_4 v[0] v[1] v[2] v[3] v[4] v[5] v[6] v[7] v[8] v[9] v[10] v[11] v[12] v[13] v[14]
+ v[15] v[16] v[17] v[18] v[19] v[20] v[21] v[22] v[23] v[24] v[25] v[26] v[27] v[28] v[29] v[30] v[31]
+ v[32] v[33] v[34] v[35] v[36] v[37] v[38] v[39] v[40] v[41] v[42] v[43] v[44] v[45] v[46] v[47] v[48]
+ v[49] v[50] v[51] v[52] v[53] v[54] v[55] v[56] v[57] v[58] v[59] v[60] v[61] v[62] v[63] gnd
*.opin
*+ v[0],v[1],v[2],v[3],v[4],v[5],v[6],v[7],v[8],v[9],v[10],v[11],v[12],v[13],v[14],v[15],v[16],v[17],v[18],v[19],v[20],v[21],v[22],v[23],v[24],v[25],v[26],v[27],v[28],v[29],v[30],v[31],v[32],v[33],v[34],v[35],v[36],v[37],v[38],v[39],v[40],v[41],v[42],v[43],v[44],v[45],v[46],v[47],v[48],v[49],v[50],v[51],v[52],v[53],v[54],v[55],v[56],v[57],v[58],v[59],v[60],v[61],v[62],v[63]
*.ipin gnd
XR7 v[6] v[7] gnd sky130_fd_pr__res_xhigh_po_1p41 L=0.5164 mult=1 m=1
XR10 v[9] v[10] gnd sky130_fd_pr__res_xhigh_po_1p41 L=0.5508 mult=1 m=1
XR17 v[16] v[17] gnd sky130_fd_pr__res_xhigh_po_1p41 L=0.5853 mult=1 m=1
XR28 v[27] v[28] gnd sky130_fd_pr__res_xhigh_po_1p41 L=0.6541 mult=1 m=1
XR31 v[30] v[31] gnd sky130_fd_pr__res_xhigh_po_1p41 L=0.6885 mult=1 m=1
XR36 v[35] v[36] gnd sky130_fd_pr__res_xhigh_po_1p41 L=0.7574 mult=1 m=1
XR37 v[36] v[37] gnd sky130_fd_pr__res_xhigh_po_1p41 L=0.723 mult=1 m=1
XR40 v[39] v[40] gnd sky130_fd_pr__res_xhigh_po_1p41 L=0.7918 mult=1 m=1
XR43 v[42] v[43] gnd sky130_fd_pr__res_xhigh_po_1p41 L=0.8263 mult=1 m=1
XR44 v[43] v[44] gnd sky130_fd_pr__res_xhigh_po_1p41 L=0.8607 mult=1 m=1
XR46 v[45] v[46] gnd sky130_fd_pr__res_xhigh_po_1p41 L=0.8951 mult=1 m=1
XR51 v[50] v[51] gnd sky130_fd_pr__res_xhigh_po_0p69 L=0.5054 mult=1 m=1
XR53 v[52] v[53] gnd sky130_fd_pr__res_xhigh_po_0p69 L=0.5391 mult=1 m=1
XR55 v[54] v[55] gnd sky130_fd_pr__res_xhigh_po_0p69 L=0.5728 mult=1 m=1
XR56 v[55] v[56] gnd sky130_fd_pr__res_xhigh_po_0p69 L=0.5897 mult=1 m=1
XR57 v[56] v[57] gnd sky130_fd_pr__res_xhigh_po_0p69 L=0.6234 mult=1 m=1
XR58 v[57] v[58] gnd sky130_fd_pr__res_xhigh_po_0p69 L=0.6402 mult=1 m=1
XR59 v[58] v[59] gnd sky130_fd_pr__res_xhigh_po_0p69 L=0.6907 mult=1 m=1
XR60 v[59] v[60] gnd sky130_fd_pr__res_xhigh_po_0p69 L=0.7244 mult=1 m=1
XR61 v[60] v[61] gnd sky130_fd_pr__res_xhigh_po_0p69 L=0.7581 mult=1 m=1
XR8 v[7] v[8] gnd sky130_fd_pr__res_xhigh_po_1p41 L=0.5164 mult=1 m=1
XR11 v[10] v[11] gnd sky130_fd_pr__res_xhigh_po_1p41 L=0.5164 mult=1 m=1
XR12 v[11] v[12] gnd sky130_fd_pr__res_xhigh_po_1p41 L=0.5508 mult=1 m=1
XR13 v[12] v[13] gnd sky130_fd_pr__res_xhigh_po_1p41 L=0.5164 mult=1 m=1
XR23 v[22] v[23] gnd sky130_fd_pr__res_xhigh_po_1p41 L=0.6197 mult=1 m=1
XR34 v[33] v[34] gnd sky130_fd_pr__res_xhigh_po_1p41 L=0.723 mult=1 m=1
XR41 v[40] v[41] gnd sky130_fd_pr__res_xhigh_po_1p41 L=0.7918 mult=1 m=1
XR1 v[0] v[1] gnd sky130_fd_pr__res_xhigh_po_2p85 L=0.9742 mult=1 m=1
XR2 v[1] v[2] gnd sky130_fd_pr__res_xhigh_po_2p85 L=0.9742 mult=1 m=1
XR4 v[3] v[4] gnd sky130_fd_pr__res_xhigh_po_2p85 L=0.9742 mult=1 m=1
XR6 v[5] v[6] gnd sky130_fd_pr__res_xhigh_po_2p85 L=0.9742 mult=1 m=1
XR3 v[2] v[3] gnd sky130_fd_pr__res_xhigh_po_2p85 L=1.0438 mult=1 m=1
XR5 v[4] v[5] gnd sky130_fd_pr__res_xhigh_po_2p85 L=1.0438 mult=1 m=1
XR9 v[8] v[9] gnd sky130_fd_pr__res_xhigh_po_1p41 L=0.5164 mult=1 m=1
XR14 v[13] v[14] gnd sky130_fd_pr__res_xhigh_po_1p41 L=0.5508 mult=1 m=1
XR15 v[14] v[15] gnd sky130_fd_pr__res_xhigh_po_1p41 L=0.5508 mult=1 m=1
XR16 v[15] v[16] gnd sky130_fd_pr__res_xhigh_po_1p41 L=0.5508 mult=1 m=1
XR18 v[17] v[18] gnd sky130_fd_pr__res_xhigh_po_1p41 L=0.5508 mult=1 m=1
XR19 v[18] v[19] gnd sky130_fd_pr__res_xhigh_po_1p41 L=0.5853 mult=1 m=1
XR20 v[19] v[20] gnd sky130_fd_pr__res_xhigh_po_1p41 L=0.5853 mult=1 m=1
XR21 v[20] v[21] gnd sky130_fd_pr__res_xhigh_po_1p41 L=0.5853 mult=1 m=1
XR22 v[21] v[22] gnd sky130_fd_pr__res_xhigh_po_1p41 L=0.5853 mult=1 m=1
XR24 v[23] v[24] gnd sky130_fd_pr__res_xhigh_po_1p41 L=0.6197 mult=1 m=1
XR25 v[24] v[25] gnd sky130_fd_pr__res_xhigh_po_1p41 L=0.6197 mult=1 m=1
XR26 v[25] v[26] gnd sky130_fd_pr__res_xhigh_po_1p41 L=0.6197 mult=1 m=1
XR27 v[26] v[27] gnd sky130_fd_pr__res_xhigh_po_1p41 L=0.6197 mult=1 m=1
XR29 v[28] v[29] gnd sky130_fd_pr__res_xhigh_po_1p41 L=0.6541 mult=1 m=1
XR30 v[29] v[30] gnd sky130_fd_pr__res_xhigh_po_1p41 L=0.6541 mult=1 m=1
XR32 v[31] v[32] gnd sky130_fd_pr__res_xhigh_po_1p41 L=0.6541 mult=1 m=1
XR33 v[32] v[33] gnd sky130_fd_pr__res_xhigh_po_1p41 L=0.6885 mult=1 m=1
XR35 v[34] v[35] gnd sky130_fd_pr__res_xhigh_po_1p41 L=0.6885 mult=1 m=1
XR38 v[37] v[38] gnd sky130_fd_pr__res_xhigh_po_1p41 L=0.7574 mult=1 m=1
XR39 v[38] v[39] gnd sky130_fd_pr__res_xhigh_po_1p41 L=0.7574 mult=1 m=1
XR42 v[41] v[42] gnd sky130_fd_pr__res_xhigh_po_1p41 L=0.7918 mult=1 m=1
XR45 v[44] v[45] gnd sky130_fd_pr__res_xhigh_po_1p41 L=0.8607 mult=1 m=1
XR47 v[46] v[47] gnd sky130_fd_pr__res_xhigh_po_1p41 L=0.8951 mult=1 m=1
XR48 v[47] v[48] gnd sky130_fd_pr__res_xhigh_po_1p41 L=0.9295 mult=1 m=1
XR49 v[48] v[49] gnd sky130_fd_pr__res_xhigh_po_1p41 L=0.964 mult=1 m=1
XR50 v[49] v[50] gnd sky130_fd_pr__res_xhigh_po_1p41 L=0.964 mult=1 m=1
XR52 v[51] v[52] gnd sky130_fd_pr__res_xhigh_po_0p69 L=0.5054 mult=1 m=1
XR54 v[53] v[54] gnd sky130_fd_pr__res_xhigh_po_0p69 L=0.5391 mult=1 m=1
XR62 v[61] v[62] gnd sky130_fd_pr__res_xhigh_po_0p69 L=0.8424 mult=1 m=1
XR63 v[62] v[63] gnd sky130_fd_pr__res_xhigh_po_0p69 L=0.8929 mult=1 m=1
.ends

.end
